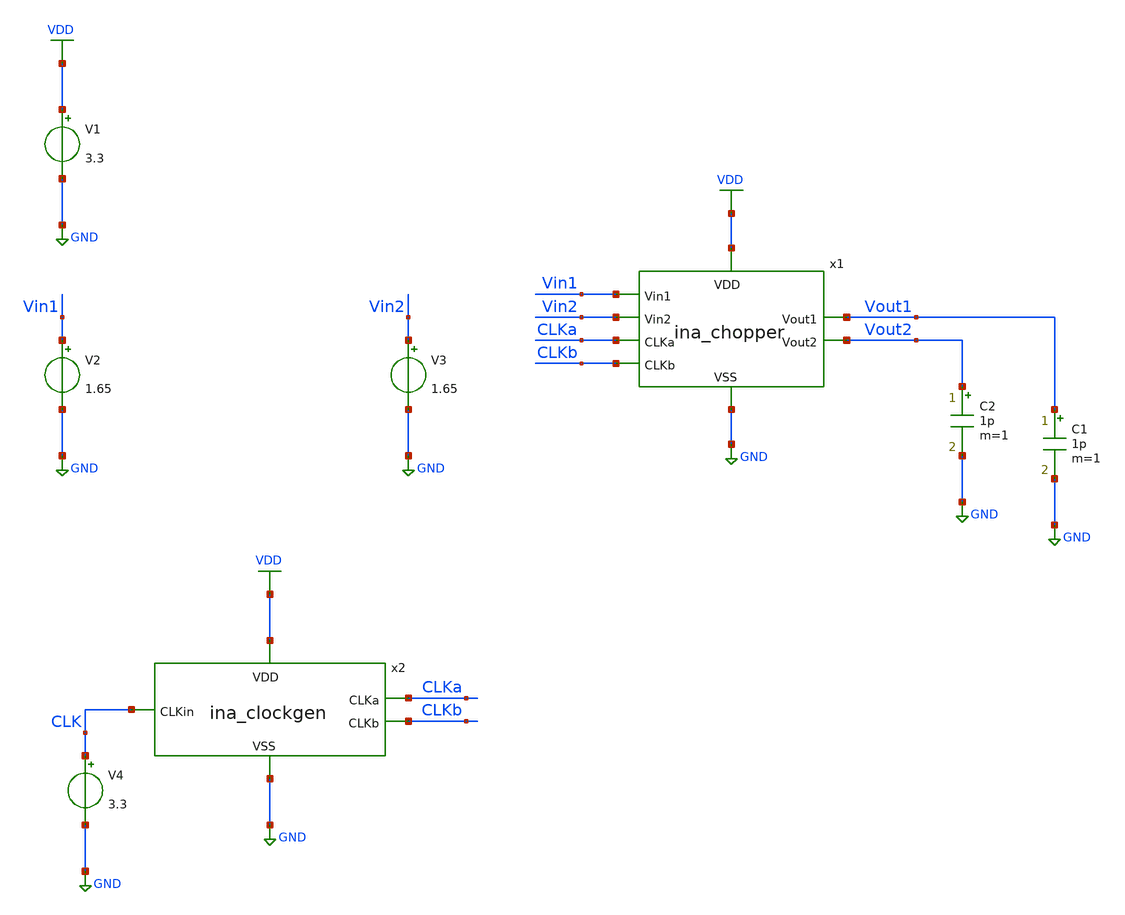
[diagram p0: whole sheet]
** sch_path: designs/libs/tb_ina/tb_ina_chopper_op/tb_ina_chopper_op.sch
**.subckt tb_ina_chopper_op
V1 VDD GND 3.3
V2 Vin1 GND 1.65
V3 Vin2 GND 1.65
C2 Vout2 GND 1p m=1
C1 Vout1 GND 1p m=1
x1 Vout2 Vin1 VDD GND CLKb CLKa Vout1 Vin2 ina_chopper
V4 CLK GND 3.3
x2 VDD CLK CLKa CLKb GND ina_clockgen
**** begin user architecture code

.include $::180MCU_MODELS/design.ngspice
.lib $::180MCU_MODELS/sm141064.ngspice typical
.lib $::180MCU_MODELS/sm141064.ngspice cap_mim
.lib $::180MCU_MODELS/sm141064.ngspice moscap_typical
.lib $::180MCU_MODELS/sm141064.ngspice mimcap_typical
.lib $::180MCU_MODELS/sm141064.ngspice res_typical
* .lib $::180MCU_MODELS/sm141064.ngspice res_statistical
* ngspice commands




.control
save all

set color0 = white

*************************************
** PARAMETERS
*************************************

let Vdd  = 3.3
let Vcm  = 1.65

*************************************
** SOURCES
*************************************

alter @V1[DC] = $&Vdd
alter @V2[DC] = $&Vcm
alter @V3[DC] = $&Vcm

*************************************
** TRANSMISSION GATE ON
*************************************

alter @V4[DC] = $&Vdd

*************************************
** OPERATING POINT SIMULATION
*************************************

op

*************************************
** PRINT RESULTS
*************************************

echo ------ TG ON --------
echo ------ NMOS ---------
let XM1_vgs = @m.x1.xm1.m0[vgs]
let XM1_vds = @m.x1.xm1.m0[vds]
let XM1_id = @m.x1.xm1.m0[id]
let XM1_gm = @m.x1.xm1.m0[gm]
let XM1_gds = @m.x1.xm1.m0[gds]
let XM1_cgg = @m.x1.xm1.m0[cgg]
let XM1_cgd = @m.x1.xm1.m0[cgd]
let XM1_cgs = @m.x1.xm1.m0[cgs]
let XM1_ron = 1/@m.x1.xm1.m0[gds]
print XM1_vgs
print XM1_vds
print XM1_id
print XM1_gm
print XM1_gds
print XM1_cgg
print XM1_ron
echo ------ PMOS ---------
let XM2_vgs = @m.x1.xm2.m0[vgs]
let XM2_vds = @m.x1.xm2.m0[vds]
let XM2_id = @m.x1.xm2.m0[id]
let XM2_gm = @m.x1.xm2.m0[gm]
let XM2_gds = @m.x1.xm2.m0[gds]
let XM2_cgg = @m.x1.xm2.m0[cgg]
let XM2_cgd = @m.x1.xm2.m0[cgd]
let XM2_cgs = @m.x1.xm2.m0[cgs]
let XM2_ron = 1/@m.x1.xm2.m0[gds]
print XM2_vgs
print XM2_vds
print XM2_id
print XM2_gm
print XM2_gds
print XM2_cgg
print XM2_ron
echo ------ TG -----------
let Ron1 = 1/(XM1_gds + XM2_gds)
let Roff2 = 1/(@m.x1.xm3.m0[gds] + @m.x1.xm4.m0[gds])
let Ron3 = 1/(@m.x1.xm5.m0[gds] + @m.x1.xm6.m0[gds])
let Roff4 = 1/(@m.x1.xm7.m0[gds] + @m.x1.xm8.m0[gds])
let Cin = abs(XM1_cgd)+abs(XM1_cgs)+abs(XM2_cgd)+abs(XM2_cgs)
let Ileak2 = abs(@m.x1.xm3.m0[id]) + abs(@m.x1.xm4.m0[id])
let Ileak4 = abs(@m.x1.xm7.m0[id]) + abs(@m.x1.xm8.m0[id])
let Ileak_tot = Ileak2 + Ileak4
print Ron1
print Roff2
print Ron3
print Roff4
print Cin
print Ileak2
print Ileak4
print Ileak_tot

*************************************
** SAVE
*************************************

write tb_ina_chopper_op1.raw

*************************************
** TRANSMISSION GATE OFF
*************************************

alter @V4[DC] = 0

*************************************
** OPERATING POINT SIMULATION
*************************************

op

*************************************
** PRINT RESULTS
*************************************

echo ------ TG OFF -------
echo ------ NMOS ---------
let XM1_vgs = @m.x1.xm1.m0[vgs]
let XM1_vds = @m.x1.xm1.m0[vds]
let XM1_id = @m.x1.xm1.m0[id]
let XM1_gm = @m.x1.xm1.m0[gm]
let XM1_gds = @m.x1.xm1.m0[gds]
let XM1_cgg = @m.x1.xm1.m0[cgg]
let XM1_roff = 1/@m.x1.xm1.m0[gds]
print XM1_vgs
print XM1_vds
print XM1_id
print XM1_gm
print XM1_gds
print XM1_cgg
print XM1_roff
echo ------ PMOS ---------
let XM2_vgs = @m.x1.xm2.m0[vgs]
let XM2_vds = @m.x1.xm2.m0[vds]
let XM2_id = @m.x1.xm2.m0[id]
let XM2_gm = @m.x1.xm2.m0[gm]
let XM2_gds = @m.x1.xm2.m0[gds]
let XM2_cgg = @m.x1.xm2.m0[cgg]
let XM2_roff = 1/@m.x1.xm2.m0[gds]
print XM2_vgs
print XM2_vds
print XM2_id
print XM2_gm
print XM2_gds
print XM2_cgg
print XM2_roff
echo ------ TG -----------
let Roff1 = 1/(XM1_gds + XM2_gds)
let Ron2 = 1/(@m.x1.xm3.m0[gds] + @m.x1.xm4.m0[gds])
let Roff3 = 1/(@m.x1.xm5.m0[gds] + @m.x1.xm6.m0[gds])
let Ron4 = 1/(@m.x1.xm7.m0[gds] + @m.x1.xm8.m0[gds])
let Ileak1 = abs(@m.x1.xm1.m0[id]) + abs(@m.x1.xm2.m0[id])
let Ileak3 = abs(@m.x1.xm5.m0[id]) + abs(@m.x1.xm6.m0[id])
let Ileak_tot = Ileak1 + Ileak3
print Roff1
print Ron2
print Roff3
print Ron4
print Ileak1
print Ileak3
print Ileak_tot

*************************************
** SAVE
*************************************

write tb_ina_chopper_op2.raw

.endc
* ngspice commands



**** end user architecture code
**.ends

* expanding   symbol:  libs/core_ina/ina_chopper/ina_chopper.sym # of pins=8
** sym_path: designs/libs/core_ina/ina_chopper/ina_chopper.sym
** sch_path: designs/libs/core_ina/ina_chopper/ina_chopper.sch
.subckt ina_chopper Vout2 Vin1 VDD VSS CLKb CLKa Vout1 Vin2
*.ipin Vin1
*.ipin Vin2
*.ipin CLKb
*.opin Vout2
*.ipin CLKa
*.opin Vout1
*.ipin VDD
*.ipin VSS
XM1 Vout1 CLKa Vin1 VSS nfet_03v3 L=0.28u W=2u nf=1 ad='int((nf+1)/2) * W/nf * 0.18u' as='int((nf+2)/2) * W/nf * 0.18u'
+ pd='2*int((nf+1)/2) * (W/nf + 0.18u)' ps='2*int((nf+2)/2) * (W/nf + 0.18u)' nrd='0.18u / W' nrs='0.18u / W'
+ sa=0 sb=0 sd=0 m=1
XM2 Vout1 CLKb Vin1 VDD pfet_03v3 L=0.28u W=2u nf=1 ad='int((nf+1)/2) * W/nf * 0.18u' as='int((nf+2)/2) * W/nf * 0.18u'
+ pd='2*int((nf+1)/2) * (W/nf + 0.18u)' ps='2*int((nf+2)/2) * (W/nf + 0.18u)' nrd='0.18u / W' nrs='0.18u / W'
+ sa=0 sb=0 sd=0 m=2
XM3 Vout2 CLKb Vin1 VSS nfet_03v3 L=0.28u W=2u nf=1 ad='int((nf+1)/2) * W/nf * 0.18u' as='int((nf+2)/2) * W/nf * 0.18u'
+ pd='2*int((nf+1)/2) * (W/nf + 0.18u)' ps='2*int((nf+2)/2) * (W/nf + 0.18u)' nrd='0.18u / W' nrs='0.18u / W'
+ sa=0 sb=0 sd=0 m=1
XM4 Vout2 CLKa Vin1 VDD pfet_03v3 L=0.28u W=2u nf=1 ad='int((nf+1)/2) * W/nf * 0.18u' as='int((nf+2)/2) * W/nf * 0.18u'
+ pd='2*int((nf+1)/2) * (W/nf + 0.18u)' ps='2*int((nf+2)/2) * (W/nf + 0.18u)' nrd='0.18u / W' nrs='0.18u / W'
+ sa=0 sb=0 sd=0 m=2
XM5 Vin2 CLKa Vout2 VSS nfet_03v3 L=0.28u W=2u nf=1 ad='int((nf+1)/2) * W/nf * 0.18u' as='int((nf+2)/2) * W/nf * 0.18u'
+ pd='2*int((nf+1)/2) * (W/nf + 0.18u)' ps='2*int((nf+2)/2) * (W/nf + 0.18u)' nrd='0.18u / W' nrs='0.18u / W'
+ sa=0 sb=0 sd=0 m=1
XM6 Vin2 CLKb Vout2 VDD pfet_03v3 L=0.28u W=2u nf=1 ad='int((nf+1)/2) * W/nf * 0.18u' as='int((nf+2)/2) * W/nf * 0.18u'
+ pd='2*int((nf+1)/2) * (W/nf + 0.18u)' ps='2*int((nf+2)/2) * (W/nf + 0.18u)' nrd='0.18u / W' nrs='0.18u / W'
+ sa=0 sb=0 sd=0 m=2
XM7 Vin2 CLKb Vout1 VSS nfet_03v3 L=0.28u W=2u nf=1 ad='int((nf+1)/2) * W/nf * 0.18u' as='int((nf+2)/2) * W/nf * 0.18u'
+ pd='2*int((nf+1)/2) * (W/nf + 0.18u)' ps='2*int((nf+2)/2) * (W/nf + 0.18u)' nrd='0.18u / W' nrs='0.18u / W'
+ sa=0 sb=0 sd=0 m=1
XM8 Vin2 CLKa Vout1 VDD pfet_03v3 L=0.28u W=2u nf=1 ad='int((nf+1)/2) * W/nf * 0.18u' as='int((nf+2)/2) * W/nf * 0.18u'
+ pd='2*int((nf+1)/2) * (W/nf + 0.18u)' ps='2*int((nf+2)/2) * (W/nf + 0.18u)' nrd='0.18u / W' nrs='0.18u / W'
+ sa=0 sb=0 sd=0 m=2
XM9 Vout1 CLKb Vout1 VSS nfet_03v3 L=0.28u W=1u nf=1 ad='int((nf+1)/2) * W/nf * 0.18u' as='int((nf+2)/2) * W/nf * 0.18u'
+ pd='2*int((nf+1)/2) * (W/nf + 0.18u)' ps='2*int((nf+2)/2) * (W/nf + 0.18u)' nrd='0.18u / W' nrs='0.18u / W'
+ sa=0 sb=0 sd=0 m=1
XM10 Vout1 CLKa Vout1 VDD pfet_03v3 L=0.28u W=1u nf=1 ad='int((nf+1)/2) * W/nf * 0.18u' as='int((nf+2)/2) * W/nf * 0.18u'
+ pd='2*int((nf+1)/2) * (W/nf + 0.18u)' ps='2*int((nf+2)/2) * (W/nf + 0.18u)' nrd='0.18u / W' nrs='0.18u / W'
+ sa=0 sb=0 sd=0 m=2
XM11 Vout2 CLKa Vout2 VSS nfet_03v3 L=0.28u W=1u nf=1 ad='int((nf+1)/2) * W/nf * 0.18u' as='int((nf+2)/2) * W/nf * 0.18u'
+ pd='2*int((nf+1)/2) * (W/nf + 0.18u)' ps='2*int((nf+2)/2) * (W/nf + 0.18u)' nrd='0.18u / W' nrs='0.18u / W'
+ sa=0 sb=0 sd=0 m=1
XM12 Vout2 CLKb Vout2 VDD pfet_03v3 L=0.28u W=1u nf=1 ad='int((nf+1)/2) * W/nf * 0.18u' as='int((nf+2)/2) * W/nf * 0.18u'
+ pd='2*int((nf+1)/2) * (W/nf + 0.18u)' ps='2*int((nf+2)/2) * (W/nf + 0.18u)' nrd='0.18u / W' nrs='0.18u / W'
+ sa=0 sb=0 sd=0 m=2
XM13 Vout2 CLKa Vout2 VDD pfet_03v3 L=0.28u W=1u nf=1 ad='int((nf+1)/2) * W/nf * 0.18u' as='int((nf+2)/2) * W/nf * 0.18u'
+ pd='2*int((nf+1)/2) * (W/nf + 0.18u)' ps='2*int((nf+2)/2) * (W/nf + 0.18u)' nrd='0.18u / W' nrs='0.18u / W'
+ sa=0 sb=0 sd=0 m=2
XM14 Vout2 CLKb Vout2 VSS nfet_03v3 L=0.28u W=1u nf=1 ad='int((nf+1)/2) * W/nf * 0.18u' as='int((nf+2)/2) * W/nf * 0.18u'
+ pd='2*int((nf+1)/2) * (W/nf + 0.18u)' ps='2*int((nf+2)/2) * (W/nf + 0.18u)' nrd='0.18u / W' nrs='0.18u / W'
+ sa=0 sb=0 sd=0 m=1
XM15 Vout1 CLKb Vout1 VDD pfet_03v3 L=0.28u W=1u nf=1 ad='int((nf+1)/2) * W/nf * 0.18u' as='int((nf+2)/2) * W/nf * 0.18u'
+ pd='2*int((nf+1)/2) * (W/nf + 0.18u)' ps='2*int((nf+2)/2) * (W/nf + 0.18u)' nrd='0.18u / W' nrs='0.18u / W'
+ sa=0 sb=0 sd=0 m=2
XM16 Vout1 CLKa Vout1 VSS nfet_03v3 L=0.28u W=1u nf=1 ad='int((nf+1)/2) * W/nf * 0.18u' as='int((nf+2)/2) * W/nf * 0.18u'
+ pd='2*int((nf+1)/2) * (W/nf + 0.18u)' ps='2*int((nf+2)/2) * (W/nf + 0.18u)' nrd='0.18u / W' nrs='0.18u / W'
+ sa=0 sb=0 sd=0 m=1
.ends


* expanding   symbol:  libs/core_ina/ina_clockgen/ina_clockgen.sym # of pins=5
** sym_path: designs/libs/core_ina/ina_clockgen/ina_clockgen.sym
** sch_path: designs/libs/core_ina/ina_clockgen/ina_clockgen.sch
.subckt ina_clockgen VDD CLKin CLKa CLKb VSS
*.ipin CLKin
*.ipin VDD
*.ipin VSS
*.opin CLKa
*.opin CLKb
x1 VDD net4 CLKin net1 VSS ina_nand
x2 VDD net6 net3 net2 VSS ina_nand
x3 VDD CLKin net2 VSS ina_inv
x4 VDD net4 net5 VSS ina_inv
x5 VDD net5 net3 VSS ina_inv
x6 VDD net3 CLKa VSS ina_inv
x7 VDD net6 net7 VSS ina_inv
x8 VDD net7 net1 VSS ina_inv
x9 VDD net1 CLKb VSS ina_inv
.ends


* expanding   symbol:  libs/core_ina/ina_nand/ina_nand.sym # of pins=5
** sym_path: designs/libs/core_ina/ina_nand/ina_nand.sym
** sch_path: designs/libs/core_ina/ina_nand/ina_nand.sch
.subckt ina_nand VDD Vout Vin1 Vin2 VSS
*.ipin VDD
*.ipin Vin1
*.ipin Vin2
*.ipin VSS
*.opin Vout
XMN1 Vout Vin1 VDD VDD pfet_03v3 L=0.28u W=2u nf=1 ad='int((nf+1)/2) * W/nf * 0.18u' as='int((nf+2)/2) * W/nf * 0.18u'
+ pd='2*int((nf+1)/2) * (W/nf + 0.18u)' ps='2*int((nf+2)/2) * (W/nf + 0.18u)' nrd='0.18u / W' nrs='0.18u / W'
+ sa=0 sb=0 sd=0 m=1
XMN2 Vout Vin2 VDD VDD pfet_03v3 L=0.28u W=2u nf=1 ad='int((nf+1)/2) * W/nf * 0.18u' as='int((nf+2)/2) * W/nf * 0.18u'
+ pd='2*int((nf+1)/2) * (W/nf + 0.18u)' ps='2*int((nf+2)/2) * (W/nf + 0.18u)' nrd='0.18u / W' nrs='0.18u / W'
+ sa=0 sb=0 sd=0 m=1
XMN3 Vout Vin1 net1 VSS nfet_03v3 L=0.28u W=2u nf=1 ad='int((nf+1)/2) * W/nf * 0.18u' as='int((nf+2)/2) * W/nf * 0.18u'
+ pd='2*int((nf+1)/2) * (W/nf + 0.18u)' ps='2*int((nf+2)/2) * (W/nf + 0.18u)' nrd='0.18u / W' nrs='0.18u / W'
+ sa=0 sb=0 sd=0 m=1
XMN4 net1 Vin2 VSS VSS nfet_03v3 L=0.28u W=2u nf=1 ad='int((nf+1)/2) * W/nf * 0.18u' as='int((nf+2)/2) * W/nf * 0.18u'
+ pd='2*int((nf+1)/2) * (W/nf + 0.18u)' ps='2*int((nf+2)/2) * (W/nf + 0.18u)' nrd='0.18u / W' nrs='0.18u / W'
+ sa=0 sb=0 sd=0 m=1
.ends


* expanding   symbol:  libs/core_ina/ina_inv/ina_inv.sym # of pins=4
** sym_path: designs/libs/core_ina/ina_inv/ina_inv.sym
** sch_path: designs/libs/core_ina/ina_inv/ina_inv.sch
.subckt ina_inv VDD Vin Vout VSS
*.ipin VDD
*.ipin VSS
*.ipin Vin
*.opin Vout
XMI1 Vout Vin VDD VDD pfet_03v3 L=0.28u W=2u nf=1 ad='int((nf+1)/2) * W/nf * 0.18u' as='int((nf+2)/2) * W/nf * 0.18u'
+ pd='2*int((nf+1)/2) * (W/nf + 0.18u)' ps='2*int((nf+2)/2) * (W/nf + 0.18u)' nrd='0.18u / W' nrs='0.18u / W'
+ sa=0 sb=0 sd=0 m=1
XMI2 Vout Vin VSS VSS nfet_03v3 L=0.28u W=1u nf=1 ad='int((nf+1)/2) * W/nf * 0.18u' as='int((nf+2)/2) * W/nf * 0.18u'
+ pd='2*int((nf+1)/2) * (W/nf + 0.18u)' ps='2*int((nf+2)/2) * (W/nf + 0.18u)' nrd='0.18u / W' nrs='0.18u / W'
+ sa=0 sb=0 sd=0 m=1
.ends

.GLOBAL GND
.GLOBAL VDD
.end
